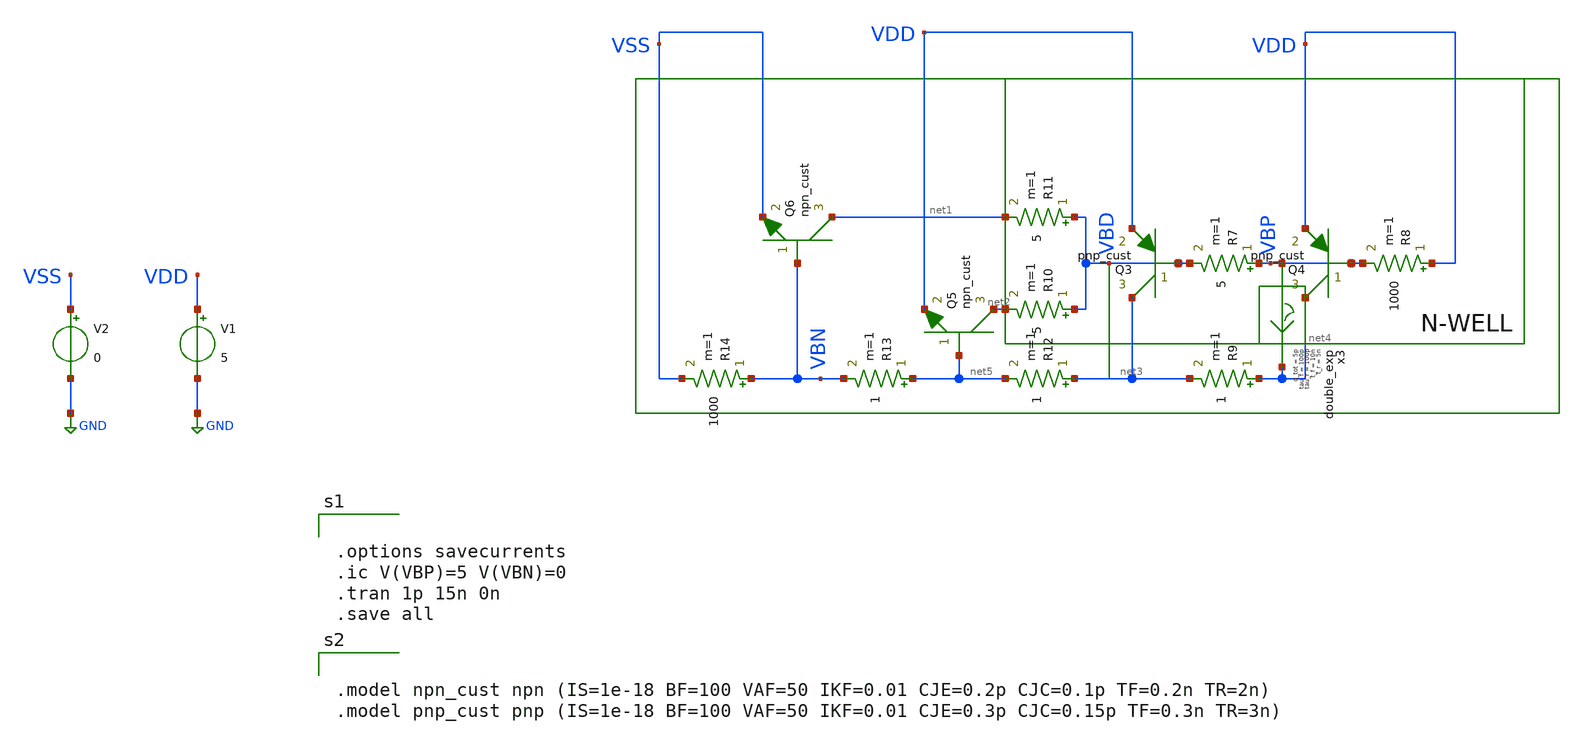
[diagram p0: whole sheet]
** sch_path: latchup/advanced_test.sch
**.subckt advanced_test
Q3 net3 VBD VDD pnp_cust area=1 m=1
Q4 net4 VBP VDD pnp_cust area=1 m=1
R7 VBP VBD 5 m=1
R8 VDD VBP 1000 m=1
R9 net4 net3 1 m=1
R10 VBD net2 5 m=1
R11 VBD net1 5 m=1
Q5 net2 net5 VDD npn_cust area=1 m=1
Q6 net1 VBN VSS npn_cust area=1 m=1
R12 net3 net5 1 m=1
R13 net5 VBN 1 m=1
R14 VBN VSS 1000 m=1
V1 VDD GND 5
V2 VSS GND 0
x3 VBP net4 double_exp t_r=5n tau_r=100p t_f=10n tau_f=100p q_tot=5p
**** begin user architecture code


.options savecurrents
.ic V(VBP)=5 V(VBN)=0
.tran 1p 15n 0n
.save all




.include /usr/local/share/rad_modeling_blocks/rad_modeling_blocks.spice




.model npn_cust npn (IS=1e-18 BF=100 VAF=50 IKF=0.01 CJE=0.2p CJC=0.1p TF=0.2n TR=2n)
.model pnp_cust pnp (IS=1e-18 BF=100 VAF=50 IKF=0.01 CJE=0.3p CJC=0.15p TF=0.3n TR=3n)


**** end user architecture code
**.ends

* expanding   symbol:  double_exp.sym # of pins=2
** sym_path: xschem_rad_library/double_exp.sym
** sch_path: xschem_rad_library/double_exp.sch
.subckt double_exp in out  t_r=0 t_f=0 tau_r=0 tau_f=0 q_tot=0
*.opin OUT
*.ipin IN
I1 IN OUT EXP(0 {q_tot / (t_f-t_r+tau_f-tau_r)} {t_r} {tau_r} {t_f} {tau_f})
.ends

.GLOBAL GND
.end
